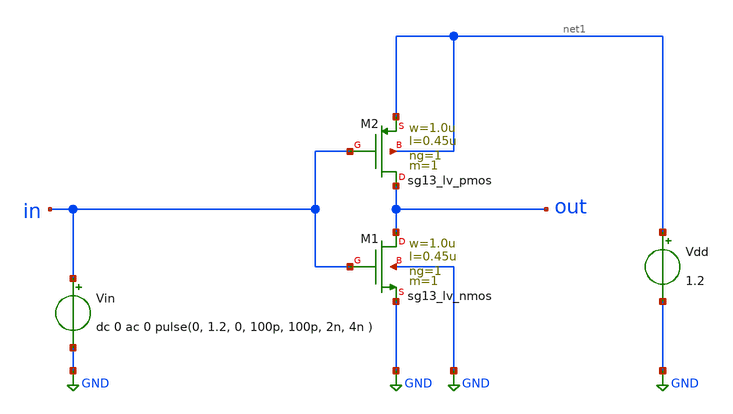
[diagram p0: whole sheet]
** sch_path: ihp-sg13g2/xschem_libs/sg13g2_tests_ase/tran_logic_not/schematic/tran_logic_not.sch
* Copyright 2023 IHP PDK Authors
**.subckt tran_logic_not
Vin in GND dc 0 ac 0 pulse(0, 1.2, 0, 100p, 100p, 2n, 4n )
Vdd net1 GND 1.2
XM1 out in GND GND sg13_lv_nmos w=1.0u l=0.45u ng=1 m=1 mm_ok=1
XM2 out in net1 net1 sg13_lv_pmos w=1.0u l=0.45u ng=1 m=1 mm_ok=1
**.ends
.GLOBAL GND
.end
